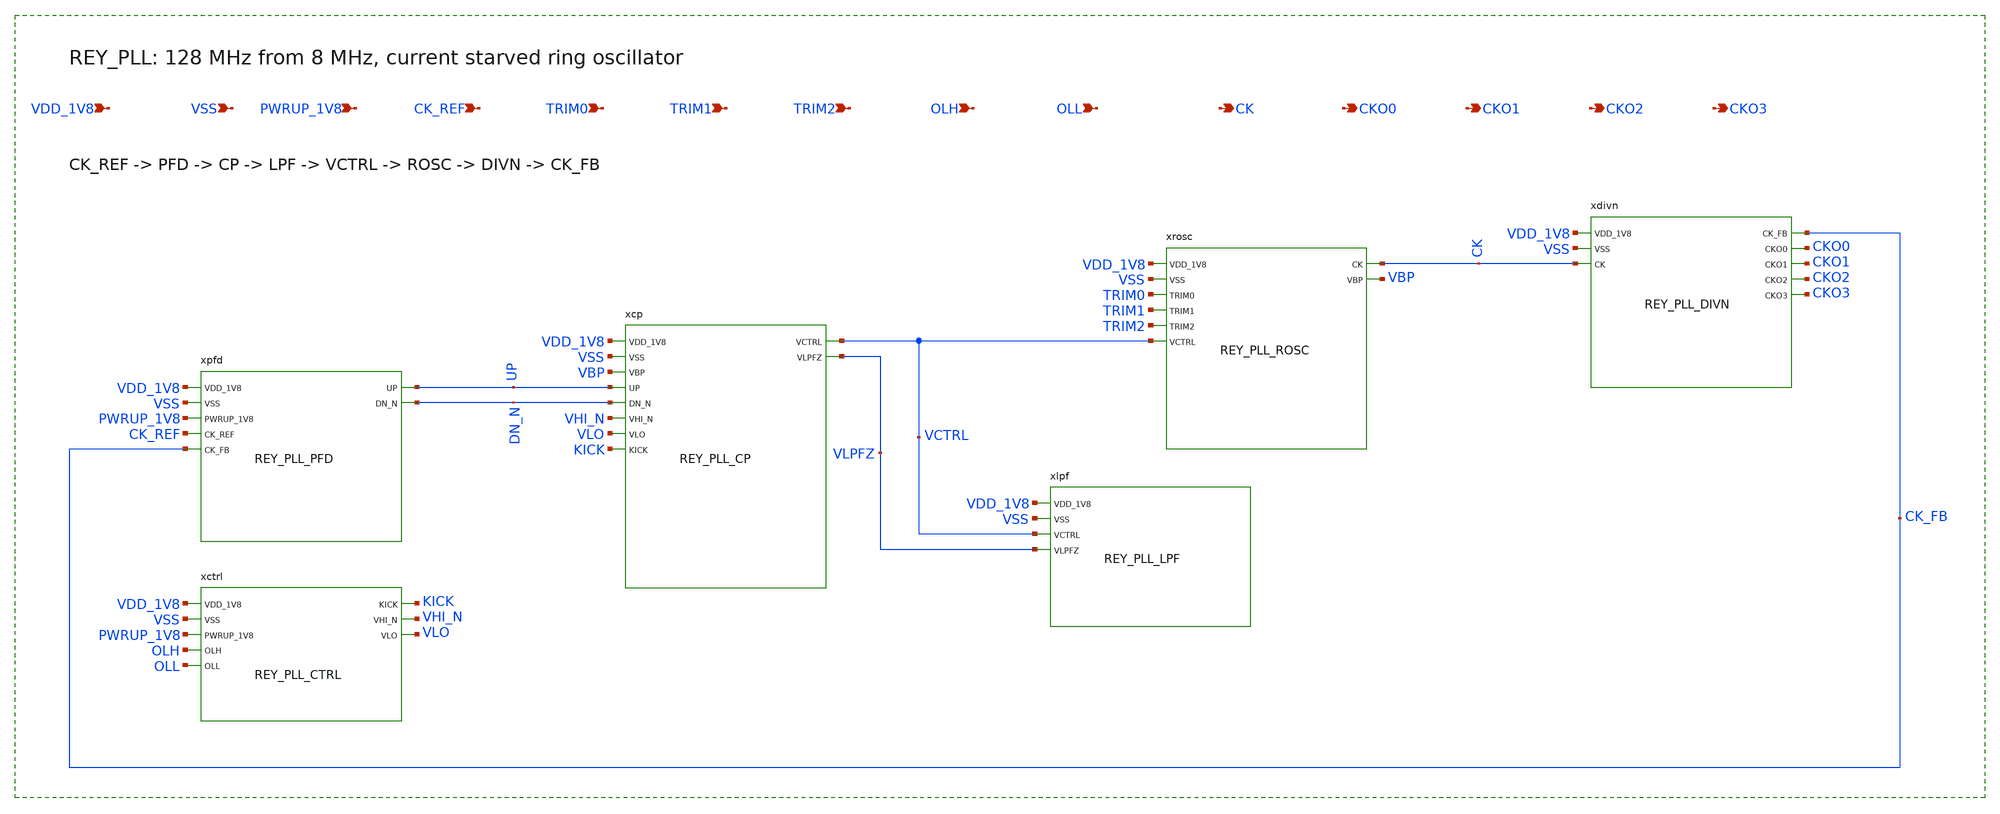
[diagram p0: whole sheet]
** sch_path: design/REY_PLL_SKY130A/REY_PLL.sch
**.subckt REY_PLL VDD_1V8 VSS PWRUP_1V8 CK_REF TRIM0 TRIM1 TRIM2 OLH OLL CK CKO0 CKO1 CKO2 CKO3
*.ipin VDD_1V8
*.ipin VSS
*.ipin PWRUP_1V8
*.ipin CK_REF
*.ipin TRIM0
*.ipin TRIM1
*.ipin TRIM2
*.ipin OLH
*.ipin OLL
*.opin CK
*.opin CKO0
*.opin CKO1
*.opin CKO2
*.opin CKO3
xctrl VDD_1V8 VSS PWRUP_1V8 OLH OLL KICK VHI_N VLO REY_PLL_CTRL
xpfd VDD_1V8 VSS PWRUP_1V8 CK_REF CK_FB UP DN_N REY_PLL_PFD
xcp VDD_1V8 VSS VBP UP DN_N VHI_N VLO KICK VCTRL VLPFZ REY_PLL_CP
xlpf VDD_1V8 VSS VCTRL VLPFZ REY_PLL_LPF
xrosc VDD_1V8 VSS TRIM0 TRIM1 TRIM2 VCTRL CK VBP REY_PLL_ROSC
xdivn VDD_1V8 VSS CK CK_FB CKO0 CKO1 CKO2 CKO3 REY_PLL_DIVN
**.ends
.end
